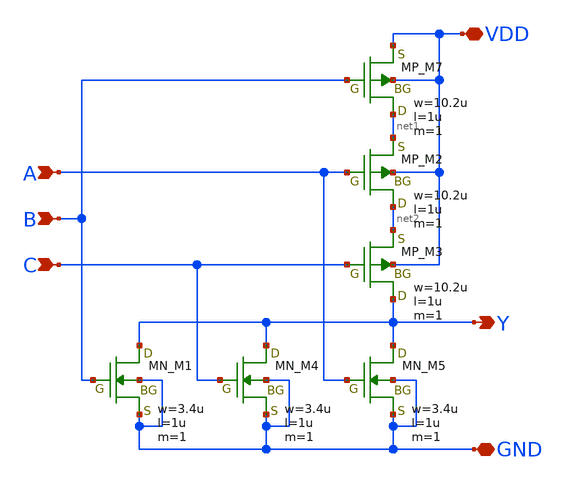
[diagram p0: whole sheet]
** sch_path: libs.tech/xschem/TR-1um_stdcell/NOR3.sch
**.subckt NOR3 A B Y VDD GND C
*.ipin A
*.ipin B
*.opin Y
*.iopin VDD
*.iopin GND
*.ipin C
XM7 net1 B VDD VDD PMOS w=10.2u l=1u nrd=0 nrs=0 m=1
XM2 net2 A net1 VDD PMOS w=10.2u l=1u nrd=0 nrs=0 m=1
XM3 Y C net2 VDD PMOS w=10.2u l=1u nrd=0 nrs=0 m=1
XM1 Y B GND GND NMOS w=3.4u l=1u nrd=0 nrs=0 m=1
XM4 Y C GND GND NMOS w=3.4u l=1u nrd=0 nrs=0 m=1
XM5 Y A GND GND NMOS w=3.4u l=1u nrd=0 nrs=0 m=1
**.ends
.end
